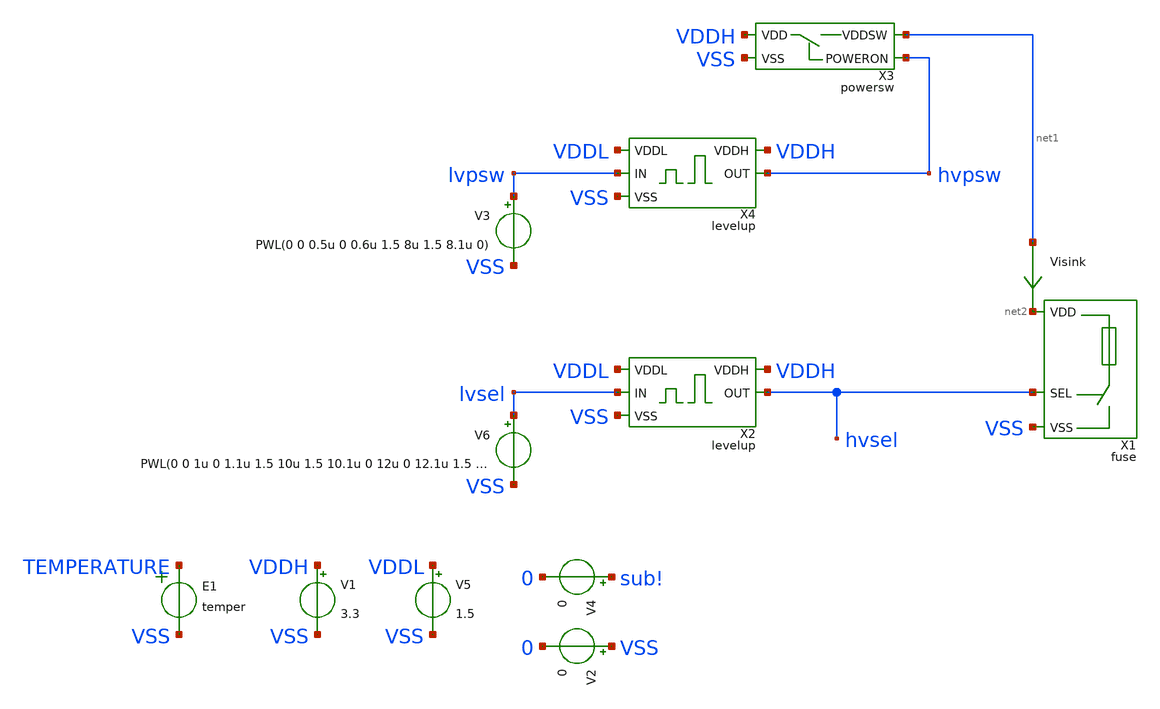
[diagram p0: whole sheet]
** sch_path: ip/util/xschem/util_tb.sch
**.subckt util_tb
V1 VDDH VSS 3.3
Visink net1 net2 0
.save i(visink)
V2 VSS 0 0
E1 TEMPERATURE VSS VOL=' temper '
V4 sub! 0 0
X1 net2 VSS hvsel fuse
V5 VDDL VSS 1.5
X2 VDDL VSS lvsel VDDH hvsel levelup
V6 lvsel VSS PWL(0 0 1u 0 1.1u 1.5 10u 1.5 10.1u 0 12u 0 12.1u 1.5 15u 1.5 15.1u 0)
X4 VDDL VSS lvpsw VDDH hvpsw levelup
V3 lvpsw VSS PWL(0 0 0.5u 0 0.6u 1.5 8u 1.5 8.1u 0)
X3 VDDH hvpsw net1 VSS powersw
**** begin user architecture code


.csparam TB_ID=${::TB_ID}
.csparam MC_RUNS=${::MC_RUNS}
.csparam EXIT_NGSPICE=${::EXIT_NGSPICE}
.lib ${::IHP_MODELS}/sg13g2.lib ${::CORNER}




.control
* option savecurrents
save all


* dummy block for goto
if (1)
if TB_ID = 0
	goto TRAN_SW
end
if TB_ID = 1
	goto TRAN_SW
end

****************************************
label TRAN_SW
****************************************
if MC_RUNS = 0
	tran 10n 17u
	plot visink#branch
	plot lvsel, hvsel
	plot lvpsw, hvpsw
else
	tran 10n 12u
	plot visink#branch
end
goto done

****************************************
label done
****************************************
if EXIT_NGSPICE > 0.0
	exit
end
end
.endc


**** end user architecture code
**.ends

* expanding   symbol:  fuse.sym # of pins=3
** sym_path: ip/util/xschem/fuse.sym
** sch_path: ip/util/xschem/fuse.sch
.subckt fuse VDD VSS SEL
*.iopin VSS
*.iopin VDD
*.ipin SEL
XM1 net1 SEL VSS VSS sg13_hv_nmos w=10u l=0.5u ng=1 m=40 mm_ok=1
X1 VDD net1 fuse_prim
.ends


* expanding   symbol:  levelup.sym # of pins=5
** sym_path: ip/util/xschem/levelup.sym
** sch_path: ip/util/xschem/levelup.sch
.subckt levelup VDDL VSS IN VDDH OUT
*.iopin VSS
*.iopin VDDL
*.ipin IN
*.iopin VDDH
*.opin OUT
XM1 net2 INB VSS VSS sg13_hv_nmos w=2u l=0.5u ng=1 m=1 mm_ok=1
XM2 INB IN VSS VSS sg13_lv_nmos w=2.75u l=0.13u ng=1 m=1 mm_ok=1
XM3 INB IN VDDL VDDL sg13_lv_pmos w=4.61u l=0.13u ng=1 m=1 mm_ok=1
XM4 net3 net1 VSS VSS sg13_hv_nmos w=2u l=0.5u ng=1 m=1 mm_ok=1
XM5 net1 INB VSS VSS sg13_lv_nmos w=2.75u l=0.13u ng=1 m=1 mm_ok=1
XM6 net1 INB VDDL VDDL sg13_lv_pmos w=4.61u l=0.13u ng=1 m=1 mm_ok=1
XM7 net3 net2 VDDH VDDH sg13_hv_pmos w=0.3u l=0.5u ng=1 m=1 mm_ok=1
XM8 net2 net3 VDDH VDDH sg13_hv_pmos w=0.3u l=0.5u ng=1 m=1 mm_ok=1
XM9 OUT net3 VDDH VDDH sg13_hv_pmos w=4u l=0.5u ng=1 m=1 mm_ok=1
XM10 OUT net3 VSS VSS sg13_hv_nmos w=2u l=0.5u ng=1 m=1 mm_ok=1
.ends


* expanding   symbol:  powersw.sym # of pins=4
** sym_path: ip/util/xschem/powersw.sym
** sch_path: ip/util/xschem/powersw.sch
.subckt powersw VDD POWERON VDDSW VSS
*.iopin VDD
*.ipin POWERON
*.iopin VDDSW
*.iopin VSS
XM2 VDDSW net1 VDD VDD sg13_hv_pmos w=60u l=0.5u ng=1 m=30 mm_ok=1
XM1 net1 POWERON VSS VSS sg13_hv_nmos w=0.5u l=2u ng=1 m=1 mm_ok=1
XR2 POWERON VSS VSS rhigh w=0.5e-6 l=80e-6 m=1 b=0 mm_ok=1
XM3 net1 POWERON VDD VDD sg13_hv_pmos w=0.5u l=4u ng=1 m=1 mm_ok=1
.ends


* expanding   symbol:  fuse_prim.sym # of pins=2
** sym_path: ip/util/xschem/fuse_prim.sym
** sch_path: ip/util/xschem/fuse_prim.sch
.subckt fuse_prim T1 T2
*.iopin T2
*.iopin T1
R1 T1 T2 50 m=1
.ends

.GLOBAL sub!
.end
